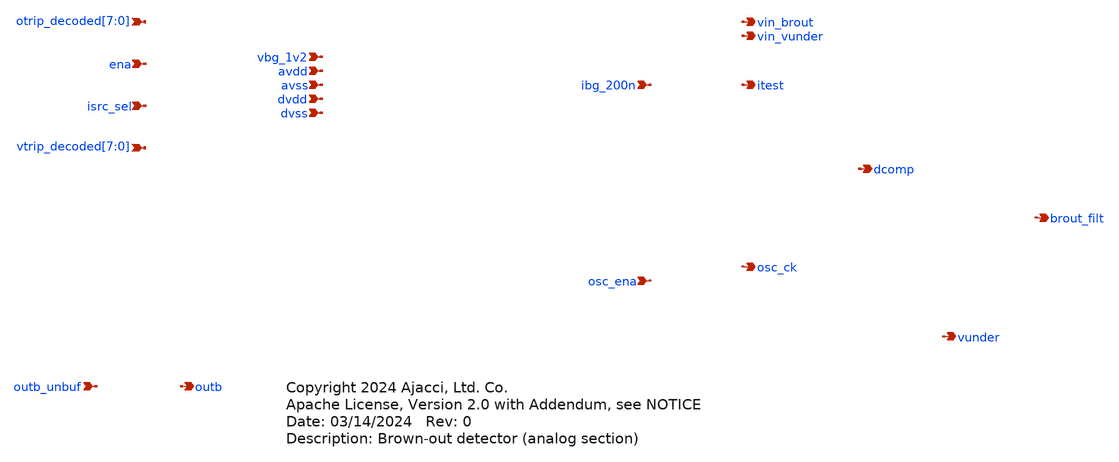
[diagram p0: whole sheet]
** sch_path: xschem/brownout_ana_rcx.sch
* Copyright 2024 Ajacci, Ltd. Co.
* Apache License, Version 2.0 with Addendum, see NOTICE
**.subckt brownout_ana_rcx vbg_1v2 avdd avss dvdd dvss ena isrc_sel ibg_200n dcomp itest osc_ena
*+ osc_ck
*+ otrip_decoded[7],otrip_decoded[6],otrip_decoded[5],otrip_decoded[4],otrip_decoded[3],otrip_decoded[2],otrip_decoded[1],otrip_decoded[0] vin_brout outb_unbuf outb vunder
*+ vtrip_decoded[7],vtrip_decoded[6],vtrip_decoded[5],vtrip_decoded[4],vtrip_decoded[3],vtrip_decoded[2],vtrip_decoded[1],vtrip_decoded[0] vin_vunder brout_filt
*.ipin vbg_1v2
*.ipin avdd
*.ipin avss
*.ipin dvdd
*.ipin dvss
*.ipin ena
*.ipin isrc_sel
*.ipin ibg_200n
*.opin dcomp
*.opin itest
*.ipin osc_ena
*.opin osc_ck
*.ipin
*+ otrip_decoded[7],otrip_decoded[6],otrip_decoded[5],otrip_decoded[4],otrip_decoded[3],otrip_decoded[2],otrip_decoded[1],otrip_decoded[0]
*.opin vin_brout
*.ipin outb_unbuf
*.opin outb
*.opin vunder
*.ipin
*+ vtrip_decoded[7],vtrip_decoded[6],vtrip_decoded[5],vtrip_decoded[4],vtrip_decoded[3],vtrip_decoded[2],vtrip_decoded[1],vtrip_decoded[0]
*.opin vin_vunder
*.opin brout_filt
**** begin user architecture code



.include mag/rcx/brownout_ana_rcx.spice

xIana vin_brout otrip_decoded[7] otrip_decoded[6] otrip_decoded[5] otrip_decoded[4] otrip_decoded[3]
+ otrip_decoded[2]  otrip_decoded[1] otrip_decoded[0] vin_vunder vbg_1v2 ena avdd ibg_200n itest avss dvdd isrc_sel
+ dvss vtrip_decoded[7] vtrip_decoded[6]  vtrip_decoded[5] vtrip_decoded[4] vtrip_decoded[3]
+ vtrip_decoded[2] vtrip_decoded[1] vtrip_decoded[0] dcomp brout_filt osc_ck osc_ena vunder outb  outb_unbuf
+ brownout_ana



**** end user architecture code
**.ends
.end
